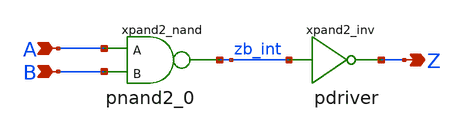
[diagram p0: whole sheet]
** sch_path: sram_2_64_scn4m_lcc/pand2.sch
**.subckt pand2 A B Z
*.ipin A
*.ipin B
*.opin Z
xpand2_nand A B zb_int vdd gnd pnand2_0
xpand2_inv zb_int Z vdd gnd pdriver
**** begin user architecture code


**** end user architecture code
**.ends
.end
